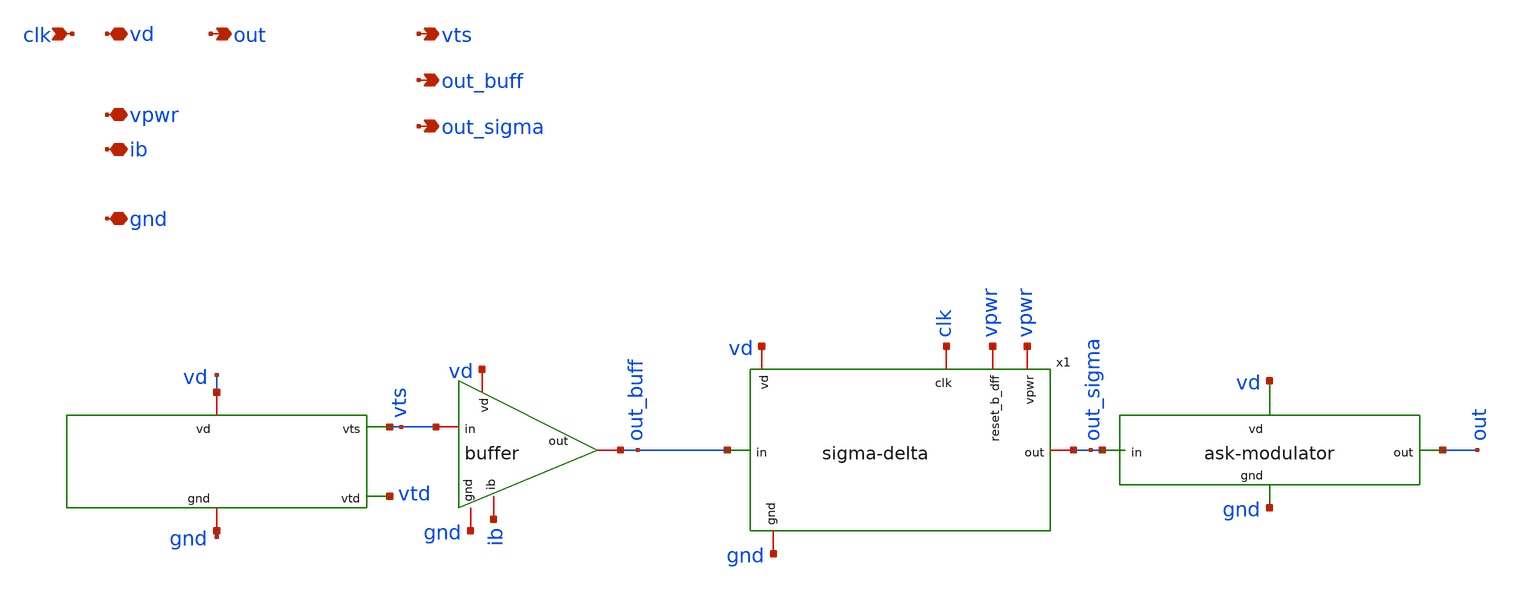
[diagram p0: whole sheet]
** sch_path: device-complete/xschem/device-complete.sch
**.subckt device-complete vd clk out vpwr ib gnd vts out_buff out_sigma
*.iopin vd
*.ipin clk
*.opin out
*.iopin vpwr
*.iopin ib
*.iopin gnd
*.opin vts
*.opin out_buff
*.opin out_sigma
x3 vd vts vtd gnd sensor
X2 vd vts out_buff ib gnd buffer
x1 vpwr clk out_sigma out_buff vpwr gnd vd sigma-delta
x4 vd out out_sigma gnd ask-modulator
**.ends
.end
